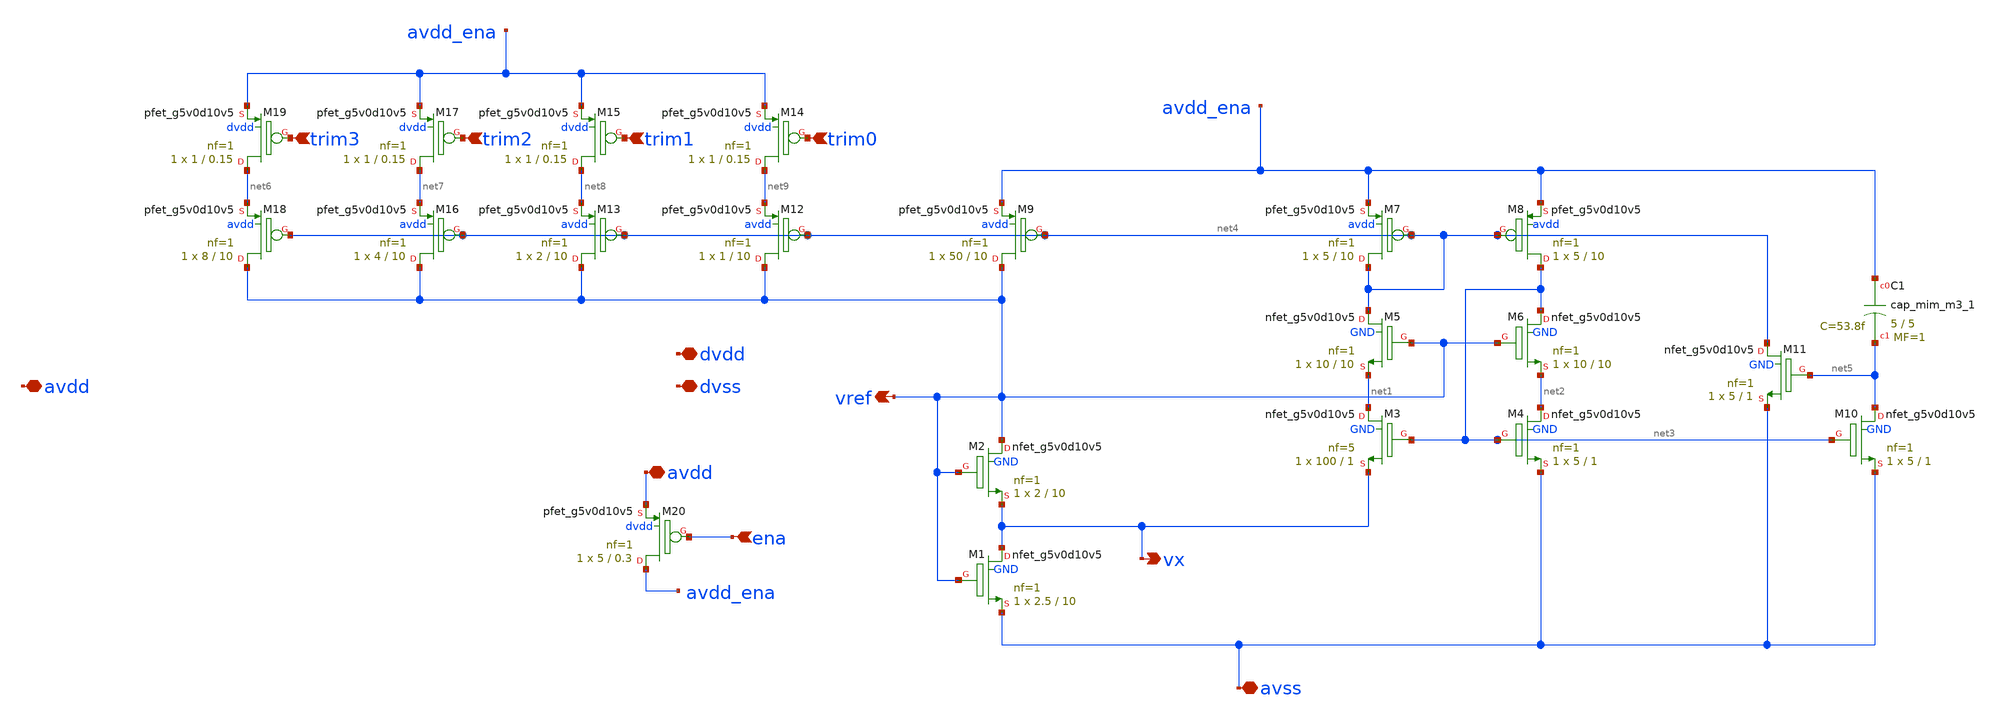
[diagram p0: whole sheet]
** sch_path: xschem/sky130_ak_ip__cmos_vref.sch
**.subckt sky130_ak_ip__cmos_vref vref avss avdd vx trim0 trim1 trim2 trim3 dvdd dvss avdd ena
*.opin vref
*.iopin avss
*.iopin avdd
*.opin vx
*.ipin trim0
*.ipin trim1
*.ipin trim2
*.ipin trim3
*.iopin dvdd
*.iopin dvss
*.iopin avdd
*.ipin ena
XM3 net1 net3 vx GND sky130_fd_pr__nfet_g5v0d10v5 L=1 W=100 nf=5 ad='int((nf+1)/2) * W/nf * 0.29' as='int((nf+2)/2) * W/nf * 0.29'
+ pd='2*int((nf+1)/2) * (W/nf + 0.29)' ps='2*int((nf+2)/2) * (W/nf + 0.29)' nrd='0.29 / W' nrs='0.29 / W'
+ sa=0 sb=0 sd=0 mult=1 m=1
XM4 net2 net3 avss GND sky130_fd_pr__nfet_g5v0d10v5 L=1 W=5 nf=1 ad='int((nf+1)/2) * W/nf * 0.29' as='int((nf+2)/2) * W/nf * 0.29'
+ pd='2*int((nf+1)/2) * (W/nf + 0.29)' ps='2*int((nf+2)/2) * (W/nf + 0.29)' nrd='0.29 / W' nrs='0.29 / W'
+ sa=0 sb=0 sd=0 mult=1 m=1
XM5 net4 vref net1 GND sky130_fd_pr__nfet_g5v0d10v5 L=10 W=10 nf=1 ad='int((nf+1)/2) * W/nf * 0.29' as='int((nf+2)/2) * W/nf * 0.29'
+ pd='2*int((nf+1)/2) * (W/nf + 0.29)' ps='2*int((nf+2)/2) * (W/nf + 0.29)' nrd='0.29 / W' nrs='0.29 / W'
+ sa=0 sb=0 sd=0 mult=1 m=1
XM6 net3 vref net2 GND sky130_fd_pr__nfet_g5v0d10v5 L=10 W=10 nf=1 ad='int((nf+1)/2) * W/nf * 0.29' as='int((nf+2)/2) * W/nf * 0.29'
+ pd='2*int((nf+1)/2) * (W/nf + 0.29)' ps='2*int((nf+2)/2) * (W/nf + 0.29)' nrd='0.29 / W' nrs='0.29 / W'
+ sa=0 sb=0 sd=0 mult=1 m=1
XM7 net4 net4 avdd_ena avdd sky130_fd_pr__pfet_g5v0d10v5 L=10 W=5 nf=1 ad='int((nf+1)/2) * W/nf * 0.29'
+ as='int((nf+2)/2) * W/nf * 0.29' pd='2*int((nf+1)/2) * (W/nf + 0.29)' ps='2*int((nf+2)/2) * (W/nf + 0.29)'
+ nrd='0.29 / W' nrs='0.29 / W' sa=0 sb=0 sd=0 mult=1 m=1
XM8 net3 net4 avdd_ena avdd sky130_fd_pr__pfet_g5v0d10v5 L=10 W=5 nf=1 ad='int((nf+1)/2) * W/nf * 0.29'
+ as='int((nf+2)/2) * W/nf * 0.29' pd='2*int((nf+1)/2) * (W/nf + 0.29)' ps='2*int((nf+2)/2) * (W/nf + 0.29)'
+ nrd='0.29 / W' nrs='0.29 / W' sa=0 sb=0 sd=0 mult=1 m=1
XM9 vref net4 avdd_ena avdd sky130_fd_pr__pfet_g5v0d10v5 L=10 W=50 nf=1 ad='int((nf+1)/2) * W/nf * 0.29'
+ as='int((nf+2)/2) * W/nf * 0.29' pd='2*int((nf+1)/2) * (W/nf + 0.29)' ps='2*int((nf+2)/2) * (W/nf + 0.29)'
+ nrd='0.29 / W' nrs='0.29 / W' sa=0 sb=0 sd=0 mult=1 m=1
XM10 net5 net3 avss GND sky130_fd_pr__nfet_g5v0d10v5 L=1 W=5 nf=1 ad='int((nf+1)/2) * W/nf * 0.29' as='int((nf+2)/2) * W/nf * 0.29'
+ pd='2*int((nf+1)/2) * (W/nf + 0.29)' ps='2*int((nf+2)/2) * (W/nf + 0.29)' nrd='0.29 / W' nrs='0.29 / W'
+ sa=0 sb=0 sd=0 mult=1 m=1
XM11 net4 net5 avss GND sky130_fd_pr__nfet_g5v0d10v5 L=1 W=5 nf=1 ad='int((nf+1)/2) * W/nf * 0.29' as='int((nf+2)/2) * W/nf * 0.29'
+ pd='2*int((nf+1)/2) * (W/nf + 0.29)' ps='2*int((nf+2)/2) * (W/nf + 0.29)' nrd='0.29 / W' nrs='0.29 / W'
+ sa=0 sb=0 sd=0 mult=1 m=1
XC1 avdd_ena net5 sky130_fd_pr__cap_mim_m3_1 W=5 L=5 MF=1 m=1
XM12 vref net4 net9 avdd sky130_fd_pr__pfet_g5v0d10v5 L=10 W=1 nf=1 ad='int((nf+1)/2) * W/nf * 0.29'
+ as='int((nf+2)/2) * W/nf * 0.29' pd='2*int((nf+1)/2) * (W/nf + 0.29)' ps='2*int((nf+2)/2) * (W/nf + 0.29)'
+ nrd='0.29 / W' nrs='0.29 / W' sa=0 sb=0 sd=0 mult=1 m=1
XM13 vref net4 net8 avdd sky130_fd_pr__pfet_g5v0d10v5 L=10 W=2 nf=1 ad='int((nf+1)/2) * W/nf * 0.29'
+ as='int((nf+2)/2) * W/nf * 0.29' pd='2*int((nf+1)/2) * (W/nf + 0.29)' ps='2*int((nf+2)/2) * (W/nf + 0.29)'
+ nrd='0.29 / W' nrs='0.29 / W' sa=0 sb=0 sd=0 mult=1 m=1
XM14 net9 trim0 avdd_ena dvdd sky130_fd_pr__pfet_g5v0d10v5 L=0.15 W=1 nf=1 ad='int((nf+1)/2) * W/nf * 0.29'
+ as='int((nf+2)/2) * W/nf * 0.29' pd='2*int((nf+1)/2) * (W/nf + 0.29)' ps='2*int((nf+2)/2) * (W/nf + 0.29)'
+ nrd='0.29 / W' nrs='0.29 / W' sa=0 sb=0 sd=0 mult=1 m=1
XM15 net8 trim1 avdd_ena dvdd sky130_fd_pr__pfet_g5v0d10v5 L=0.15 W=1 nf=1 ad='int((nf+1)/2) * W/nf * 0.29'
+ as='int((nf+2)/2) * W/nf * 0.29' pd='2*int((nf+1)/2) * (W/nf + 0.29)' ps='2*int((nf+2)/2) * (W/nf + 0.29)'
+ nrd='0.29 / W' nrs='0.29 / W' sa=0 sb=0 sd=0 mult=1 m=1
XM16 vref net4 net7 avdd sky130_fd_pr__pfet_g5v0d10v5 L=10 W=4 nf=1 ad='int((nf+1)/2) * W/nf * 0.29'
+ as='int((nf+2)/2) * W/nf * 0.29' pd='2*int((nf+1)/2) * (W/nf + 0.29)' ps='2*int((nf+2)/2) * (W/nf + 0.29)'
+ nrd='0.29 / W' nrs='0.29 / W' sa=0 sb=0 sd=0 mult=1 m=1
XM17 net7 trim2 avdd_ena dvdd sky130_fd_pr__pfet_g5v0d10v5 L=0.15 W=1 nf=1 ad='int((nf+1)/2) * W/nf * 0.29'
+ as='int((nf+2)/2) * W/nf * 0.29' pd='2*int((nf+1)/2) * (W/nf + 0.29)' ps='2*int((nf+2)/2) * (W/nf + 0.29)'
+ nrd='0.29 / W' nrs='0.29 / W' sa=0 sb=0 sd=0 mult=1 m=1
XM18 vref net4 net6 avdd sky130_fd_pr__pfet_g5v0d10v5 L=10 W=8 nf=1 ad='int((nf+1)/2) * W/nf * 0.29'
+ as='int((nf+2)/2) * W/nf * 0.29' pd='2*int((nf+1)/2) * (W/nf + 0.29)' ps='2*int((nf+2)/2) * (W/nf + 0.29)'
+ nrd='0.29 / W' nrs='0.29 / W' sa=0 sb=0 sd=0 mult=1 m=1
XM19 net6 trim3 avdd_ena dvdd sky130_fd_pr__pfet_g5v0d10v5 L=0.15 W=1 nf=1 ad='int((nf+1)/2) * W/nf * 0.29'
+ as='int((nf+2)/2) * W/nf * 0.29' pd='2*int((nf+1)/2) * (W/nf + 0.29)' ps='2*int((nf+2)/2) * (W/nf + 0.29)'
+ nrd='0.29 / W' nrs='0.29 / W' sa=0 sb=0 sd=0 mult=1 m=1
XM1 vx vref avss GND sky130_fd_pr__nfet_g5v0d10v5 L=10 W=2.5 nf=1 ad='int((nf+1)/2) * W/nf * 0.29' as='int((nf+2)/2) * W/nf * 0.29'
+ pd='2*int((nf+1)/2) * (W/nf + 0.29)' ps='2*int((nf+2)/2) * (W/nf + 0.29)' nrd='0.29 / W' nrs='0.29 / W'
+ sa=0 sb=0 sd=0 mult=1 m=1
XM2 vref vref vx GND sky130_fd_pr__nfet_g5v0d10v5 L=10 W=2 nf=1 ad='int((nf+1)/2) * W/nf * 0.29' as='int((nf+2)/2) * W/nf * 0.29'
+ pd='2*int((nf+1)/2) * (W/nf + 0.29)' ps='2*int((nf+2)/2) * (W/nf + 0.29)' nrd='0.29 / W' nrs='0.29 / W'
+ sa=0 sb=0 sd=0 mult=1 m=1
XM20 avdd_ena ena avdd dvdd sky130_fd_pr__pfet_g5v0d10v5 L=0.3 W=5 nf=1 ad='int((nf+1)/2) * W/nf * 0.29'
+ as='int((nf+2)/2) * W/nf * 0.29' pd='2*int((nf+1)/2) * (W/nf + 0.29)' ps='2*int((nf+2)/2) * (W/nf + 0.29)'
+ nrd='0.29 / W' nrs='0.29 / W' sa=0 sb=0 sd=0 mult=1 m=1
**.ends
.end
